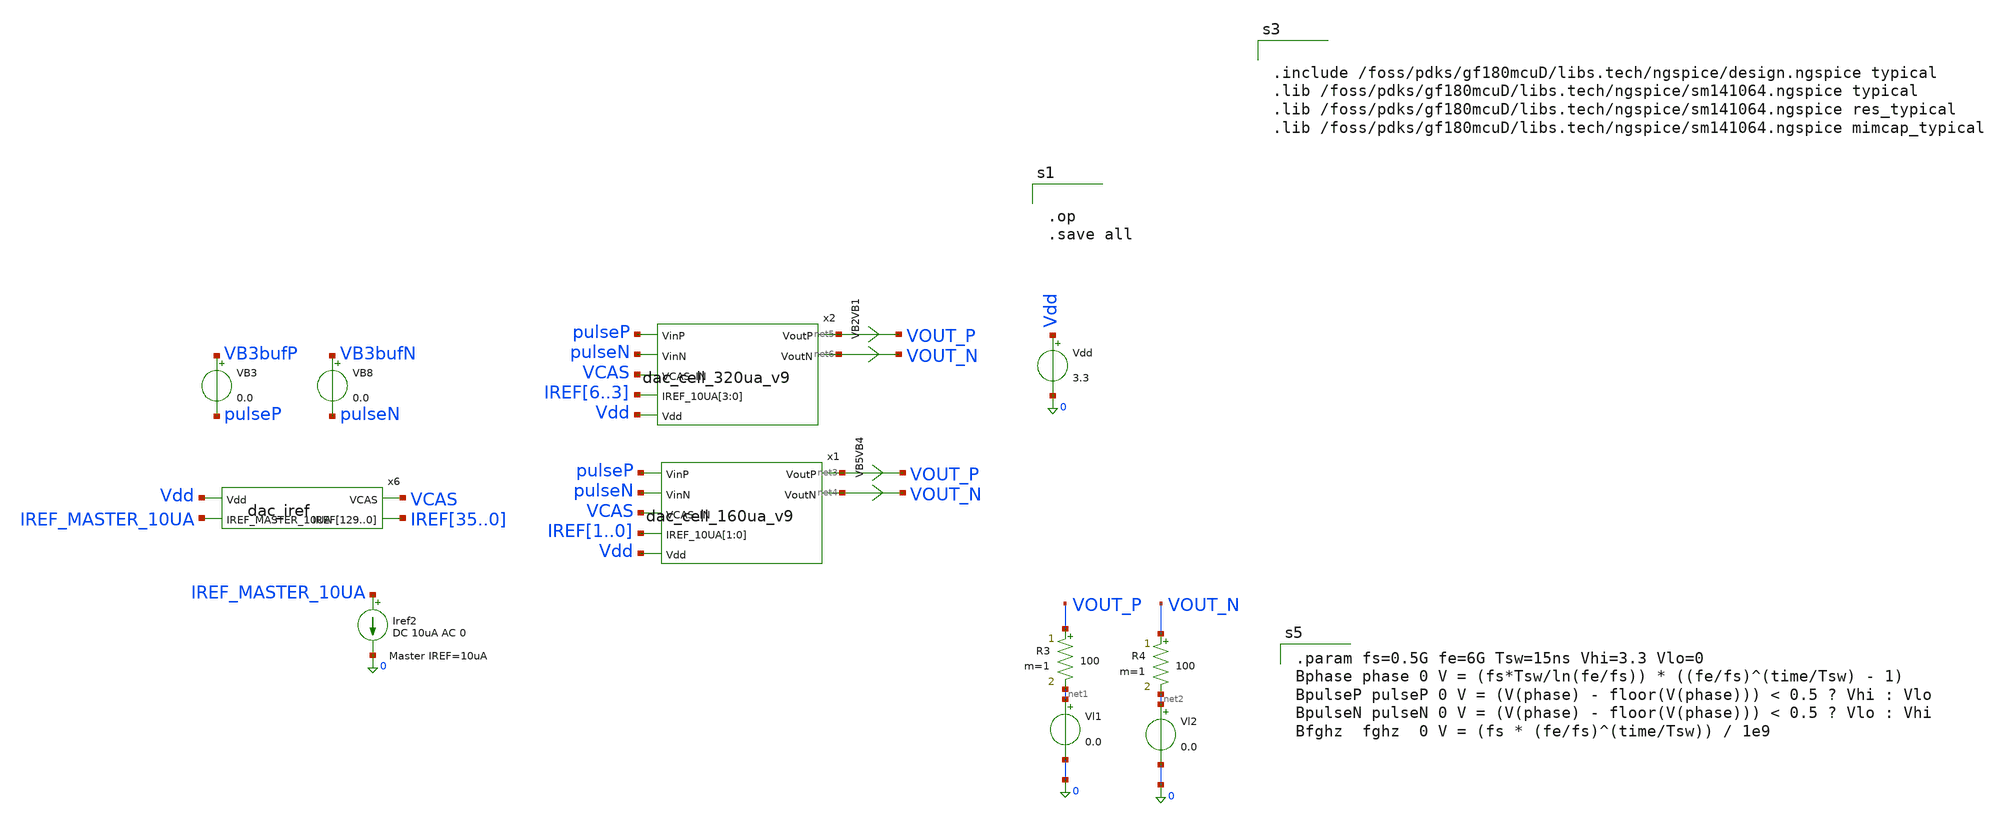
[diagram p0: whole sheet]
** sch_path: blocks/dac/test/test_dac_fsweep_160ua.sch
**.subckt test_dac_fsweep_160ua
Vdd Vdd 0 3.3
.save i(vdd)
VB3 VB3bufP pulseP 0.0
.save i(vb3)
VB8 VB3bufN pulseN 0.0
.save i(vb8)
x6 Vdd VCAS IREF35 IREF34 IREF33 IREF32 IREF31 IREF30 IREF29 IREF28 IREF27 IREF26 IREF25 IREF24
+ IREF23 IREF22 IREF21 IREF20 IREF19 IREF18 IREF17 IREF16 IREF15 IREF14 IREF13 IREF12 IREF11 IREF10 IREF9
+ IREF8 IREF7 IREF6 IREF5 IREF4 IREF3 IREF2 IREF1 IREF0 IREF35 IREF34 IREF33 IREF32 IREF31 IREF30 IREF29
+ IREF28 IREF27 IREF26 IREF25 IREF24 IREF23 IREF22 IREF21 IREF20 IREF19 IREF18 IREF17 IREF16 IREF15 IREF14
+ IREF13 IREF12 IREF11 IREF10 IREF9 IREF8 IREF7 IREF6 IREF5 IREF4 IREF3 IREF2 IREF1 IREF0 IREF35 IREF34
+ IREF33 IREF32 IREF31 IREF30 IREF29 IREF28 IREF27 IREF26 IREF25 IREF24 IREF23 IREF22 IREF21 IREF20 IREF19
+ IREF18 IREF17 IREF16 IREF15 IREF14 IREF13 IREF12 IREF11 IREF10 IREF9 IREF8 IREF7 IREF6 IREF5 IREF4 IREF3
+ IREF2 IREF1 IREF0 IREF35 IREF34 IREF33 IREF32 IREF31 IREF30 IREF29 IREF28 IREF27 IREF26 IREF25 IREF24
+ IREF23 IREF22 IREF21 IREF20 IREF19 IREF18 IREF17 IREF16 IREF15 IREF14 IREF_MASTER_10UA dac_iref
Iref2 IREF_MASTER_10UA 0 DC 10uA AC 0
R3 VOUT_P net1 100 m=1
R4 VOUT_N net2 100 m=1
Vl1 net1 0 0.0
.save i(vl1)
Vl2 net2 0 0.0
.save i(vl2)
VB4 net3 VOUT_P 0
.save i(vb4)
VB5 net4 VOUT_N 0
.save i(vb5)
x1 net3 pulseP net4 pulseN VCAS IREF1 IREF0 Vdd dac_cell_160ua_v9
VB1 net5 VOUT_P 0
.save i(vb1)
VB2 net6 VOUT_N 0
.save i(vb2)
x2 net5 pulseP net6 pulseN VCAS IREF6 IREF5 IREF4 IREF3 Vdd dac_cell_320ua_v9
**** begin user architecture code



.save all
.control

tran 1p 5ns
* plot VU1syncP+6 VU1syncN+6 VU2syncP+6 VU2syncN+6 VgN+12 VgP Dm ClkP+18 ClkN+18 i(Vl1)*5E4-6
*+ i(Vl2)*5E4-6 (i(Vl1)-i(Vl2))*5E4-12
* plot ClkP+6 ClkN+6 VU0in VB1in VU0syncP-6 VU0syncN-12 VB1syncP-6 VB1syncN-12
* plot Vout1P+15E-3 Vout1N+15E-3 Vout1P-Vout1N
* plot ClkP+5 ClkN+5 VB3syncP VB3syncN VB3bufP-5 VB3bufN-5 xb3.x1.Vg1P-10 xb3.x1.Vg1N-10
plot 3.3-xb3.x1.Vg1P 3.3-xb3.x1.Vg1N

* plot x1.x1.Vcx x1.x1.Vg1P x1.x1.Vg1N

* plot VB1syncP VB1syncN-6 VB4syncN-6 VU0bufP-12 VB1bufP-12 VB4bufP-12 VU0bufN-18 VB1bufN-18
*+ VB4bufN-18
plot i(Vl1)-i(Vl2) i(Vl1)+100E-6 i(Vl2)+100E-6

let imax = 160E-6
let imin = -160E-6
plot i(VB4)-i(VB5) imax imin
plot i(VB1)-i(VB2) i(VB4)-i(VB5) imax imin

let diff = i(Vl1)-i(Vl2)
plot pulseP diff/{imax}*5 fghz
* plot pulseP fghz



* plot i(VoutB3P)+100E-6 i(VoutB3N)+100E-6 i(VoutB3P)-i(VoutB3N) i(VoutB3N)+i(VoutB3P)
*+ i(v.x1.Vcrr1)-200E-6 i(v.x1.Vcrr2)-200E-6
* plot i(v.x1.Vcrr1) i(v.x1.Vcrr2)
* plot i(Vl1) VB1in/5E4+200E-6 VU0in/5E4+200E-6
* wrdata /foss/designs/dds/dac_isource_unary_pmos_80ua_v4_tt_500ps.csv ClkP ClkN Din VdsyncP VdsyncN
*+ i(Vl1) i(Vl2)
.endc





.op
.save all



.param fs=0.5G fe=6G Tsw=15ns Vhi=3.3 Vlo=0
Bphase phase 0 V = (fs*Tsw/ln(fe/fs)) * ((fe/fs)^(time/Tsw) - 1)
BpulseP pulseP 0 V = (V(phase) - floor(V(phase))) < 0.5 ? Vhi : Vlo
BpulseN pulseN 0 V = (V(phase) - floor(V(phase))) < 0.5 ? Vlo : Vhi
Bfghz  fghz  0 V = (fs * (fe/fs)^(time/Tsw)) / 1e9





.include /foss/pdks/gf180mcuD/libs.tech/ngspice/design.ngspice typical
.lib /foss/pdks/gf180mcuD/libs.tech/ngspice/sm141064.ngspice typical
.lib /foss/pdks/gf180mcuD/libs.tech/ngspice/sm141064.ngspice res_typical
.lib /foss/pdks/gf180mcuD/libs.tech/ngspice/sm141064.ngspice mimcap_typical


**** end user architecture code
**.ends

* expanding   symbol:  iref/dac_iref.sym # of pins=4
** sym_path: blocks/dac/iref/dac_iref.sym
** sch_path: blocks/dac/iref/dac_iref.sch
.subckt dac_iref Vdd VCAS IREF129 IREF128 IREF127 IREF126 IREF125 IREF124 IREF123 IREF122 IREF121
+ IREF120 IREF119 IREF118 IREF117 IREF116 IREF115 IREF114 IREF113 IREF112 IREF111 IREF110 IREF109 IREF108
+ IREF107 IREF106 IREF105 IREF104 IREF103 IREF102 IREF101 IREF100 IREF99 IREF98 IREF97 IREF96 IREF95 IREF94
+ IREF93 IREF92 IREF91 IREF90 IREF89 IREF88 IREF87 IREF86 IREF85 IREF84 IREF83 IREF82 IREF81 IREF80 IREF79
+ IREF78 IREF77 IREF76 IREF75 IREF74 IREF73 IREF72 IREF71 IREF70 IREF69 IREF68 IREF67 IREF66 IREF65 IREF64
+ IREF63 IREF62 IREF61 IREF60 IREF59 IREF58 IREF57 IREF56 IREF55 IREF54 IREF53 IREF52 IREF51 IREF50 IREF49
+ IREF48 IREF47 IREF46 IREF45 IREF44 IREF43 IREF42 IREF41 IREF40 IREF39 IREF38 IREF37 IREF36 IREF35 IREF34
+ IREF33 IREF32 IREF31 IREF30 IREF29 IREF28 IREF27 IREF26 IREF25 IREF24 IREF23 IREF22 IREF21 IREF20 IREF19
+ IREF18 IREF17 IREF16 IREF15 IREF14 IREF13 IREF12 IREF11 IREF10 IREF9 IREF8 IREF7 IREF6 IREF5 IREF4 IREF3
+ IREF2 IREF1 IREF0 IREF_MASTER_10UA
*.ipin Vdd
*.opin VCAS
*.opin
*+ IREF129,IREF128,IREF127,IREF126,IREF125,IREF124,IREF123,IREF122,IREF121,IREF120,IREF119,IREF118,IREF117,IREF116,IREF115,IREF114,IREF113,IREF112,IREF111,IREF110,IREF109,IREF108,IREF107,IREF106,IREF105,IREF104,IREF103,IREF102,IREF101,IREF100,IREF99,IREF98,IREF97,IREF96,IREF95,IREF94,IREF93,IREF92,IREF91,IREF90,IREF89,IREF88,IREF87,IREF86,IREF85,IREF84,IREF83,IREF82,IREF81,IREF80,IREF79,IREF78,IREF77,IREF76,IREF75,IREF74,IREF73,IREF72,IREF71,IREF70,IREF69,IREF68,IREF67,IREF66,IREF65,IREF64,IREF63,IREF62,IREF61,IREF60,IREF59,IREF58,IREF57,IREF56,IREF55,IREF54,IREF53,IREF52,IREF51,IREF50,IREF49,IREF48,IREF47,IREF46,IREF45,IREF44,IREF43,IREF42,IREF41,IREF40,IREF39,IREF38,IREF37,IREF36,IREF35,IREF34,IREF33,IREF32,IREF31,IREF30,IREF29,IREF28,IREF27,IREF26,IREF25,IREF24,IREF23,IREF22,IREF21,IREF20,IREF19,IREF18,IREF17,IREF16,IREF15,IREF14,IREF13,IREF12,IREF11,IREF10,IREF9,IREF8,IREF7,IREF6,IREF5,IREF4,IREF3,IREF2,IREF1,IREF0
*.ipin IREF_MASTER_10UA
XM69 net3 net2 0 0 nfet_03v3 L=2u W=6u nf=1 ad='int((nf+1)/2) * W/nf * 0.18u' as='int((nf+2)/2) * W/nf * 0.18u'
+ pd='2*int((nf+1)/2) * (W/nf + 0.18u)' ps='2*int((nf+2)/2) * (W/nf + 0.18u)' nrd='0.18u / W' nrs='0.18u / W'
+ sa=0 sb=0 sd=0 m=1
XM70 net2 net1 0 0 nfet_03v3 L=2u W=4u nf=1 ad='int((nf+1)/2) * W/nf * 0.18u' as='int((nf+2)/2) * W/nf * 0.18u'
+ pd='2*int((nf+1)/2) * (W/nf + 0.18u)' ps='2*int((nf+2)/2) * (W/nf + 0.18u)' nrd='0.18u / W' nrs='0.18u / W'
+ sa=0 sb=0 sd=0 m=1
XM71 net1 net4 Vdd Vdd pfet_03v3 L=2u W=6u nf=1 ad='int((nf+1)/2) * W/nf * 0.18u' as='int((nf+2)/2) * W/nf * 0.18u'
+ pd='2*int((nf+1)/2) * (W/nf + 0.18u)' ps='2*int((nf+2)/2) * (W/nf + 0.18u)' nrd='0.18u / W' nrs='0.18u / W'
+ sa=0 sb=0 sd=0 m=1
XM72 net4 net3 Vdd Vdd pfet_03v3 L=2u W=5u nf=1 ad='int((nf+1)/2) * W/nf * 0.18u' as='int((nf+2)/2) * W/nf * 0.18u'
+ pd='2*int((nf+1)/2) * (W/nf + 0.18u)' ps='2*int((nf+2)/2) * (W/nf + 0.18u)' nrd='0.18u / W' nrs='0.18u / W'
+ sa=0 sb=0 sd=0 m=1
x1 Vdd VCAS net4 VCAS IB_10UA ota5t
XC7 net4 0 cap_mim_2f0_m3m4_noshield c_width=5e-6 c_length=5e-6 m=1
XM7 VPg1 VPg1 Vdd Vdd pfet_03v3 L=1u W=6u nf=1 ad='int((nf+1)/2) * W/nf * 0.18u' as='int((nf+2)/2) * W/nf * 0.18u'
+ pd='2*int((nf+1)/2) * (W/nf + 0.18u)' ps='2*int((nf+2)/2) * (W/nf + 0.18u)' nrd='0.18u / W' nrs='0.18u / W'
+ sa=0 sb=0 sd=0 m=1
XM8 IREF_MASTER_10UA IREF_MASTER_10UA VPg1 Vdd pfet_03v3 L=1u W=6u nf=1 ad='int((nf+1)/2) * W/nf * 0.18u'
+ as='int((nf+2)/2) * W/nf * 0.18u' pd='2*int((nf+1)/2) * (W/nf + 0.18u)' ps='2*int((nf+2)/2) * (W/nf + 0.18u)'
+ nrd='0.18u / W' nrs='0.18u / W' sa=0 sb=0 sd=0 m=1
XM9 net5 VPg1 Vdd Vdd pfet_03v3 L=1u W=6u nf=1 ad='int((nf+1)/2) * W/nf * 0.18u' as='int((nf+2)/2) * W/nf * 0.18u'
+ pd='2*int((nf+1)/2) * (W/nf + 0.18u)' ps='2*int((nf+2)/2) * (W/nf + 0.18u)' nrd='0.18u / W' nrs='0.18u / W'
+ sa=0 sb=0 sd=0 m=1
XM10 VNMir IREF_MASTER_10UA net5 Vdd pfet_03v3 L=1u W=6u nf=1 ad='int((nf+1)/2) * W/nf * 0.18u' as='int((nf+2)/2) * W/nf * 0.18u'
+ pd='2*int((nf+1)/2) * (W/nf + 0.18u)' ps='2*int((nf+2)/2) * (W/nf + 0.18u)' nrd='0.18u / W' nrs='0.18u / W'
+ sa=0 sb=0 sd=0 m=1
XM11 VNMir VNMir 0 0 nfet_03v3 L=4u W=4u nf=1 ad='int((nf+1)/2) * W/nf * 0.18u' as='int((nf+2)/2) * W/nf * 0.18u'
+ pd='2*int((nf+1)/2) * (W/nf + 0.18u)' ps='2*int((nf+2)/2) * (W/nf + 0.18u)' nrd='0.18u / W' nrs='0.18u / W'
+ sa=0 sb=0 sd=0 m=1
XM12 net6 VPg1 Vdd Vdd pfet_03v3 L=1u W=6u nf=1 ad='int((nf+1)/2) * W/nf * 0.18u' as='int((nf+2)/2) * W/nf * 0.18u'
+ pd='2*int((nf+1)/2) * (W/nf + 0.18u)' ps='2*int((nf+2)/2) * (W/nf + 0.18u)' nrd='0.18u / W' nrs='0.18u / W'
+ sa=0 sb=0 sd=0 m=1
XM14 VNCas IREF_MASTER_10UA net6 Vdd pfet_03v3 L=1u W=6u nf=1 ad='int((nf+1)/2) * W/nf * 0.18u' as='int((nf+2)/2) * W/nf * 0.18u'
+ pd='2*int((nf+1)/2) * (W/nf + 0.18u)' ps='2*int((nf+2)/2) * (W/nf + 0.18u)' nrd='0.18u / W' nrs='0.18u / W'
+ sa=0 sb=0 sd=0 m=1
XM16 net7 VNCas 0 0 nfet_03v3 L={repL} W={repW} nf=1 ad='int((nf+1)/2) * W/nf * 0.18u' as='int((nf+2)/2) * W/nf * 0.18u'
+ pd='2*int((nf+1)/2) * (W/nf + 0.18u)' ps='2*int((nf+2)/2) * (W/nf + 0.18u)' nrd='0.18u / W' nrs='0.18u / W'
+ sa=0 sb=0 sd=0 m=1
XM17 VNCas VNMir net7 0 nfet_03v3 L={repL} W={repW} nf=1 ad='int((nf+1)/2) * W/nf * 0.18u' as='int((nf+2)/2) * W/nf * 0.18u'
+ pd='2*int((nf+1)/2) * (W/nf + 0.18u)' ps='2*int((nf+2)/2) * (W/nf + 0.18u)' nrd='0.18u / W' nrs='0.18u / W'
+ sa=0 sb=0 sd=0 m=1
XM4 net9 VNMir net8 0 nfet_03v3 L={repL} W={repW} nf=1 ad='int((nf+1)/2) * W/nf * 0.18u' as='int((nf+2)/2) * W/nf * 0.18u'
+ pd='2*int((nf+1)/2) * (W/nf + 0.18u)' ps='2*int((nf+2)/2) * (W/nf + 0.18u)' nrd='0.18u / W' nrs='0.18u / W'
+ sa=0 sb=0 sd=0 m=1
XM5 net9 net9 Vdd Vdd pfet_03v3 L=1u W=8u nf=1 ad='int((nf+1)/2) * W/nf * 0.18u' as='int((nf+2)/2) * W/nf * 0.18u'
+ pd='2*int((nf+1)/2) * (W/nf + 0.18u)' ps='2*int((nf+2)/2) * (W/nf + 0.18u)' nrd='0.18u / W' nrs='0.18u / W'
+ sa=0 sb=0 sd=0 m=1
XM13 net8 VNCas 0 0 nfet_03v3 L={repL} W={repW} nf=1 ad='int((nf+1)/2) * W/nf * 0.18u' as='int((nf+2)/2) * W/nf * 0.18u'
+ pd='2*int((nf+1)/2) * (W/nf + 0.18u)' ps='2*int((nf+2)/2) * (W/nf + 0.18u)' nrd='0.18u / W' nrs='0.18u / W'
+ sa=0 sb=0 sd=0 m=1
XR3 net4 net3 Vdd ppolyf_u_1k r_width=1e-6 r_length=4e-6 m=1
XR2 net1 net2 Vdd ppolyf_u_1k r_width=1e-6 r_length=8e-6 m=1
.param repW=4u
.param repL=1u
XM15 IB_10UA net9 Vdd Vdd pfet_03v3 L=1u W=8u nf=1 ad='int((nf+1)/2) * W/nf * 0.18u' as='int((nf+2)/2) * W/nf * 0.18u'
+ pd='2*int((nf+1)/2) * (W/nf + 0.18u)' ps='2*int((nf+2)/2) * (W/nf + 0.18u)' nrd='0.18u / W' nrs='0.18u / W'
+ sa=0 sb=0 sd=0 m=2
x2[129] VNMir IREF129 VNCas dac_mirror
x2[128] VNMir IREF128 VNCas dac_mirror
x2[127] VNMir IREF127 VNCas dac_mirror
x2[126] VNMir IREF126 VNCas dac_mirror
x2[125] VNMir IREF125 VNCas dac_mirror
x2[124] VNMir IREF124 VNCas dac_mirror
x2[123] VNMir IREF123 VNCas dac_mirror
x2[122] VNMir IREF122 VNCas dac_mirror
x2[121] VNMir IREF121 VNCas dac_mirror
x2[120] VNMir IREF120 VNCas dac_mirror
x2[119] VNMir IREF119 VNCas dac_mirror
x2[118] VNMir IREF118 VNCas dac_mirror
x2[117] VNMir IREF117 VNCas dac_mirror
x2[116] VNMir IREF116 VNCas dac_mirror
x2[115] VNMir IREF115 VNCas dac_mirror
x2[114] VNMir IREF114 VNCas dac_mirror
x2[113] VNMir IREF113 VNCas dac_mirror
x2[112] VNMir IREF112 VNCas dac_mirror
x2[111] VNMir IREF111 VNCas dac_mirror
x2[110] VNMir IREF110 VNCas dac_mirror
x2[109] VNMir IREF109 VNCas dac_mirror
x2[108] VNMir IREF108 VNCas dac_mirror
x2[107] VNMir IREF107 VNCas dac_mirror
x2[106] VNMir IREF106 VNCas dac_mirror
x2[105] VNMir IREF105 VNCas dac_mirror
x2[104] VNMir IREF104 VNCas dac_mirror
x2[103] VNMir IREF103 VNCas dac_mirror
x2[102] VNMir IREF102 VNCas dac_mirror
x2[101] VNMir IREF101 VNCas dac_mirror
x2[100] VNMir IREF100 VNCas dac_mirror
x2[99] VNMir IREF99 VNCas dac_mirror
x2[98] VNMir IREF98 VNCas dac_mirror
x2[97] VNMir IREF97 VNCas dac_mirror
x2[96] VNMir IREF96 VNCas dac_mirror
x2[95] VNMir IREF95 VNCas dac_mirror
x2[94] VNMir IREF94 VNCas dac_mirror
x2[93] VNMir IREF93 VNCas dac_mirror
x2[92] VNMir IREF92 VNCas dac_mirror
x2[91] VNMir IREF91 VNCas dac_mirror
x2[90] VNMir IREF90 VNCas dac_mirror
x2[89] VNMir IREF89 VNCas dac_mirror
x2[88] VNMir IREF88 VNCas dac_mirror
x2[87] VNMir IREF87 VNCas dac_mirror
x2[86] VNMir IREF86 VNCas dac_mirror
x2[85] VNMir IREF85 VNCas dac_mirror
x2[84] VNMir IREF84 VNCas dac_mirror
x2[83] VNMir IREF83 VNCas dac_mirror
x2[82] VNMir IREF82 VNCas dac_mirror
x2[81] VNMir IREF81 VNCas dac_mirror
x2[80] VNMir IREF80 VNCas dac_mirror
x2[79] VNMir IREF79 VNCas dac_mirror
x2[78] VNMir IREF78 VNCas dac_mirror
x2[77] VNMir IREF77 VNCas dac_mirror
x2[76] VNMir IREF76 VNCas dac_mirror
x2[75] VNMir IREF75 VNCas dac_mirror
x2[74] VNMir IREF74 VNCas dac_mirror
x2[73] VNMir IREF73 VNCas dac_mirror
x2[72] VNMir IREF72 VNCas dac_mirror
x2[71] VNMir IREF71 VNCas dac_mirror
x2[70] VNMir IREF70 VNCas dac_mirror
x2[69] VNMir IREF69 VNCas dac_mirror
x2[68] VNMir IREF68 VNCas dac_mirror
x2[67] VNMir IREF67 VNCas dac_mirror
x2[66] VNMir IREF66 VNCas dac_mirror
x2[65] VNMir IREF65 VNCas dac_mirror
x2[64] VNMir IREF64 VNCas dac_mirror
x2[63] VNMir IREF63 VNCas dac_mirror
x2[62] VNMir IREF62 VNCas dac_mirror
x2[61] VNMir IREF61 VNCas dac_mirror
x2[60] VNMir IREF60 VNCas dac_mirror
x2[59] VNMir IREF59 VNCas dac_mirror
x2[58] VNMir IREF58 VNCas dac_mirror
x2[57] VNMir IREF57 VNCas dac_mirror
x2[56] VNMir IREF56 VNCas dac_mirror
x2[55] VNMir IREF55 VNCas dac_mirror
x2[54] VNMir IREF54 VNCas dac_mirror
x2[53] VNMir IREF53 VNCas dac_mirror
x2[52] VNMir IREF52 VNCas dac_mirror
x2[51] VNMir IREF51 VNCas dac_mirror
x2[50] VNMir IREF50 VNCas dac_mirror
x2[49] VNMir IREF49 VNCas dac_mirror
x2[48] VNMir IREF48 VNCas dac_mirror
x2[47] VNMir IREF47 VNCas dac_mirror
x2[46] VNMir IREF46 VNCas dac_mirror
x2[45] VNMir IREF45 VNCas dac_mirror
x2[44] VNMir IREF44 VNCas dac_mirror
x2[43] VNMir IREF43 VNCas dac_mirror
x2[42] VNMir IREF42 VNCas dac_mirror
x2[41] VNMir IREF41 VNCas dac_mirror
x2[40] VNMir IREF40 VNCas dac_mirror
x2[39] VNMir IREF39 VNCas dac_mirror
x2[38] VNMir IREF38 VNCas dac_mirror
x2[37] VNMir IREF37 VNCas dac_mirror
x2[36] VNMir IREF36 VNCas dac_mirror
x2[35] VNMir IREF35 VNCas dac_mirror
x2[34] VNMir IREF34 VNCas dac_mirror
x2[33] VNMir IREF33 VNCas dac_mirror
x2[32] VNMir IREF32 VNCas dac_mirror
x2[31] VNMir IREF31 VNCas dac_mirror
x2[30] VNMir IREF30 VNCas dac_mirror
x2[29] VNMir IREF29 VNCas dac_mirror
x2[28] VNMir IREF28 VNCas dac_mirror
x2[27] VNMir IREF27 VNCas dac_mirror
x2[26] VNMir IREF26 VNCas dac_mirror
x2[25] VNMir IREF25 VNCas dac_mirror
x2[24] VNMir IREF24 VNCas dac_mirror
x2[23] VNMir IREF23 VNCas dac_mirror
x2[22] VNMir IREF22 VNCas dac_mirror
x2[21] VNMir IREF21 VNCas dac_mirror
x2[20] VNMir IREF20 VNCas dac_mirror
x2[19] VNMir IREF19 VNCas dac_mirror
x2[18] VNMir IREF18 VNCas dac_mirror
x2[17] VNMir IREF17 VNCas dac_mirror
x2[16] VNMir IREF16 VNCas dac_mirror
x2[15] VNMir IREF15 VNCas dac_mirror
x2[14] VNMir IREF14 VNCas dac_mirror
x2[13] VNMir IREF13 VNCas dac_mirror
x2[12] VNMir IREF12 VNCas dac_mirror
x2[11] VNMir IREF11 VNCas dac_mirror
x2[10] VNMir IREF10 VNCas dac_mirror
x2[9] VNMir IREF9 VNCas dac_mirror
x2[8] VNMir IREF8 VNCas dac_mirror
x2[7] VNMir IREF7 VNCas dac_mirror
x2[6] VNMir IREF6 VNCas dac_mirror
x2[5] VNMir IREF5 VNCas dac_mirror
x2[4] VNMir IREF4 VNCas dac_mirror
x2[3] VNMir IREF3 VNCas dac_mirror
x2[2] VNMir IREF2 VNCas dac_mirror
x2[1] VNMir IREF1 VNCas dac_mirror
x2[0] VNMir IREF0 VNCas dac_mirror
.ends


* expanding   symbol:  cellv9/dac_cell_160ua_v9.sym # of pins=7
** sym_path: blocks/dac/cellv9/dac_cell_160ua_v9.sym
** sch_path: blocks/dac/cellv9/dac_cell_160ua_v9.sch
.subckt dac_cell_160ua_v9 VoutP VinP VoutN VinN VCAS_IN IREF_10UA[1] IREF_10UA[0] Vdd
*.opin VoutP
*.opin VoutN
*.ipin VinP
*.ipin VinN
*.ipin Vdd
*.ipin VCAS_IN
*.ipin IREF_10UA[1],IREF_10UA[0]
x1[1] net1[1] net2[1] net3[1] net4[1] net5[1] net6[1] net7[1] net8[1] dac_cell_80ua_v9
x1[0] net1[0] net2[0] net3[0] net4[0] net5[0] net6[0] net7[0] net8[0] dac_cell_80ua_v9
.ends


* expanding   symbol:  cellv9/dac_cell_320ua_v9.sym # of pins=7
** sym_path: blocks/dac/cellv9/dac_cell_320ua_v9.sym
** sch_path: blocks/dac/cellv9/dac_cell_320ua_v9.sch
.subckt dac_cell_320ua_v9 VoutP VinP VoutN VinN VCAS_IN IREF_10UA[3] IREF_10UA[2] IREF_10UA[1]
+ IREF_10UA[0] Vdd
*.opin VoutP
*.opin VoutN
*.ipin VinP
*.ipin VinN
*.ipin Vdd
*.ipin VCAS_IN
*.ipin IREF_10UA[3],IREF_10UA[2],IREF_10UA[1],IREF_10UA[0]
x1[3] net1[3] net2[3] net3[3] net4[3] net5[3] net6[3] net7[3] net8[3] dac_cell_80ua_v9
x1[2] net1[2] net2[2] net3[2] net4[2] net5[2] net6[2] net7[2] net8[2] dac_cell_80ua_v9
x1[1] net1[1] net2[1] net3[1] net4[1] net5[1] net6[1] net7[1] net8[1] dac_cell_80ua_v9
x1[0] net1[0] net2[0] net3[0] net4[0] net5[0] net6[0] net7[0] net8[0] dac_cell_80ua_v9
.ends


* expanding   symbol:  common/ota5t.sym # of pins=5
** sym_path: blocks/dac/common/ota5t.sym
** sch_path: blocks/dac/common/ota5t.sch
.subckt ota5t Vdd VIN_N VIN_P VOUT IB_10UA
*.ipin VIN_P
*.ipin VIN_N
*.opin VOUT
*.ipin Vdd
*.ipin IB_10UA
XM16 VOUT net1 0 0 nfet_03v3 L=1u W=2u nf=1 ad='int((nf+1)/2) * W/nf * 0.18u' as='int((nf+2)/2) * W/nf * 0.18u'
+ pd='2*int((nf+1)/2) * (W/nf + 0.18u)' ps='2*int((nf+2)/2) * (W/nf + 0.18u)' nrd='0.18u / W' nrs='0.18u / W'
+ sa=0 sb=0 sd=0 m=1
XM1 VOUT VIN_N IB_10UA Vdd pfet_03v3 L=1u W=4u nf=1 ad='int((nf+1)/2) * W/nf * 0.18u' as='int((nf+2)/2) * W/nf * 0.18u'
+ pd='2*int((nf+1)/2) * (W/nf + 0.18u)' ps='2*int((nf+2)/2) * (W/nf + 0.18u)' nrd='0.18u / W' nrs='0.18u / W'
+ sa=0 sb=0 sd=0 m=1
XM19 net1 VIN_P IB_10UA Vdd pfet_03v3 L=1u W=4u nf=1 ad='int((nf+1)/2) * W/nf * 0.18u' as='int((nf+2)/2) * W/nf * 0.18u'
+ pd='2*int((nf+1)/2) * (W/nf + 0.18u)' ps='2*int((nf+2)/2) * (W/nf + 0.18u)' nrd='0.18u / W' nrs='0.18u / W'
+ sa=0 sb=0 sd=0 m=1
XM22 net1 net1 0 0 nfet_03v3 L=1u W=2u nf=1 ad='int((nf+1)/2) * W/nf * 0.18u' as='int((nf+2)/2) * W/nf * 0.18u'
+ pd='2*int((nf+1)/2) * (W/nf + 0.18u)' ps='2*int((nf+2)/2) * (W/nf + 0.18u)' nrd='0.18u / W' nrs='0.18u / W'
+ sa=0 sb=0 sd=0 m=1
.ends


* expanding   symbol:  iref/dac_mirror.sym # of pins=3
** sym_path: blocks/dac/iref/dac_mirror.sym
** sch_path: blocks/dac/iref/dac_mirror.sch
.subckt dac_mirror VN_MIR IREF VN_CAS
*.ipin VN_MIR
*.opin IREF
*.ipin VN_CAS
XM1 IREF VN_MIR net1 0 nfet_03v3 L={repL} W={repW} nf=1 ad='int((nf+1)/2) * W/nf * 0.18u' as='int((nf+2)/2) * W/nf * 0.18u'
+ pd='2*int((nf+1)/2) * (W/nf + 0.18u)' ps='2*int((nf+2)/2) * (W/nf + 0.18u)' nrd='0.18u / W' nrs='0.18u / W'
+ sa=0 sb=0 sd=0 m=1
XM2 net1 VN_CAS 0 0 nfet_03v3 L={repL} W={repW} nf=1 ad='int((nf+1)/2) * W/nf * 0.18u' as='int((nf+2)/2) * W/nf * 0.18u'
+ pd='2*int((nf+1)/2) * (W/nf + 0.18u)' ps='2*int((nf+2)/2) * (W/nf + 0.18u)' nrd='0.18u / W' nrs='0.18u / W'
+ sa=0 sb=0 sd=0 m=1
.ends


* expanding   symbol:  cellv9/dac_cell_80ua_v9.sym # of pins=8
** sym_path: blocks/dac/cellv9/dac_cell_80ua_v9.sym
** sch_path: blocks/dac/cellv9/dac_cell_80ua_v9.sch
.subckt dac_cell_80ua_v9 VoutP VinP VoutN VinN VPCas VNCas VNMir Vdd
*.opin VoutP
*.opin VoutN
*.ipin VinP
*.ipin VinN
*.ipin Vdd
*.ipin VPCas
*.ipin VNCas
*.ipin VNMir
.param cmLw=0.4u
.param cmHw=0.7u
.param cmLfbw=1.0u
.param cmHfbw=0.22u
XM20 VxP Vg1P Vcx Vdd pfet_03v3 L=0.28u W={cswW} nf=1 ad='int((nf+1)/2) * W/nf * 0.18u' as='int((nf+2)/2) * W/nf * 0.18u'
+ pd='2*int((nf+1)/2) * (W/nf + 0.18u)' ps='2*int((nf+2)/2) * (W/nf + 0.18u)' nrd='0.18u / W' nrs='0.18u / W'
+ sa=0 sb=0 sd=0 m=1
XM21 VxN Vg1N Vcx Vdd pfet_03v3 L=0.28u W={cswW} nf=1 ad='int((nf+1)/2) * W/nf * 0.18u' as='int((nf+2)/2) * W/nf * 0.18u'
+ pd='2*int((nf+1)/2) * (W/nf + 0.18u)' ps='2*int((nf+2)/2) * (W/nf + 0.18u)' nrd='0.18u / W' nrs='0.18u / W'
+ sa=0 sb=0 sd=0 m=1
XM22 VoutP VcbP VxP Vdd pfet_03v3 L=0.28u W={cbufW} nf=1 ad='int((nf+1)/2) * W/nf * 0.18u' as='int((nf+2)/2) * W/nf * 0.18u'
+ pd='2*int((nf+1)/2) * (W/nf + 0.18u)' ps='2*int((nf+2)/2) * (W/nf + 0.18u)' nrd='0.18u / W' nrs='0.18u / W'
+ sa=0 sb=0 sd=0 m=1
XM23 VoutN VcbN VxN Vdd pfet_03v3 L=0.28u W={cbufW} nf=1 ad='int((nf+1)/2) * W/nf * 0.18u' as='int((nf+2)/2) * W/nf * 0.18u'
+ pd='2*int((nf+1)/2) * (W/nf + 0.18u)' ps='2*int((nf+2)/2) * (W/nf + 0.18u)' nrd='0.18u / W' nrs='0.18u / W'
+ sa=0 sb=0 sd=0 m=1
XM24 net1 Vg1N Vdd Vdd pfet_03v3 L=0.28u W={invPw} nf=1 ad='int((nf+1)/2) * W/nf * 0.18u' as='int((nf+2)/2) * W/nf * 0.18u'
+ pd='2*int((nf+1)/2) * (W/nf + 0.18u)' ps='2*int((nf+2)/2) * (W/nf + 0.18u)' nrd='0.18u / W' nrs='0.18u / W'
+ sa=0 sb=0 sd=0 m=1
XM34 net1 Vg1N 0 0 nfet_03v3 L=0.28u W=0.22u nf=1 ad='int((nf+1)/2) * W/nf * 0.18u' as='int((nf+2)/2) * W/nf * 0.18u'
+ pd='2*int((nf+1)/2) * (W/nf + 0.18u)' ps='2*int((nf+2)/2) * (W/nf + 0.18u)' nrd='0.18u / W' nrs='0.18u / W'
+ sa=0 sb=0 sd=0 m=1
XM35 VoutN net1 VoutN Vdd pfet_03v3 L=0.28u W={dummyW} nf=1 ad='int((nf+1)/2) * W/nf * 0.18u' as='int((nf+2)/2) * W/nf * 0.18u'
+ pd='2*int((nf+1)/2) * (W/nf + 0.18u)' ps='2*int((nf+2)/2) * (W/nf + 0.18u)' nrd='0.18u / W' nrs='0.18u / W'
+ sa=0 sb=0 sd=0 m=1
XM36 net2 Vg1P Vdd Vdd pfet_03v3 L=0.28u W={invPw} nf=1 ad='int((nf+1)/2) * W/nf * 0.18u' as='int((nf+2)/2) * W/nf * 0.18u'
+ pd='2*int((nf+1)/2) * (W/nf + 0.18u)' ps='2*int((nf+2)/2) * (W/nf + 0.18u)' nrd='0.18u / W' nrs='0.18u / W'
+ sa=0 sb=0 sd=0 m=1
XM37 net2 Vg1P 0 0 nfet_03v3 L=0.28u W=0.22u nf=1 ad='int((nf+1)/2) * W/nf * 0.18u' as='int((nf+2)/2) * W/nf * 0.18u'
+ pd='2*int((nf+1)/2) * (W/nf + 0.18u)' ps='2*int((nf+2)/2) * (W/nf + 0.18u)' nrd='0.18u / W' nrs='0.18u / W'
+ sa=0 sb=0 sd=0 m=1
XM38 VoutP net2 VoutP Vdd pfet_03v3 L=0.28u W={dummyW} nf=1 ad='int((nf+1)/2) * W/nf * 0.18u' as='int((nf+2)/2) * W/nf * 0.18u'
+ pd='2*int((nf+1)/2) * (W/nf + 0.18u)' ps='2*int((nf+2)/2) * (W/nf + 0.18u)' nrd='0.18u / W' nrs='0.18u / W'
+ sa=0 sb=0 sd=0 m=1
VcbRef3 VcbRef 0 {Vcbias}
.save i(vcbref3)
.param VcBias=0.84
.param casW=4u
XM39 net3 VinPDr VH Vdd pfet_03v3 L=0.28u W={cmHw} nf=1 ad='int((nf+1)/2) * W/nf * 0.18u' as='int((nf+2)/2) * W/nf * 0.18u'
+ pd='2*int((nf+1)/2) * (W/nf + 0.18u)' ps='2*int((nf+2)/2) * (W/nf + 0.18u)' nrd='0.18u / W' nrs='0.18u / W'
+ sa=0 sb=0 sd=0 m=1
XM40 Vg1P VinPDr net3 Vdd pfet_03v3 L=0.28u W={cmHw} nf=1 ad='int((nf+1)/2) * W/nf * 0.18u' as='int((nf+2)/2) * W/nf * 0.18u'
+ pd='2*int((nf+1)/2) * (W/nf + 0.18u)' ps='2*int((nf+2)/2) * (W/nf + 0.18u)' nrd='0.18u / W' nrs='0.18u / W'
+ sa=0 sb=0 sd=0 m=1
XM41 Vg1P VinPDr VL 0 nfet_03v3 L=0.28u W={cmLw} nf=1 ad='int((nf+1)/2) * W/nf * 0.18u' as='int((nf+2)/2) * W/nf * 0.18u'
+ pd='2*int((nf+1)/2) * (W/nf + 0.18u)' ps='2*int((nf+2)/2) * (W/nf + 0.18u)' nrd='0.18u / W' nrs='0.18u / W'
+ sa=0 sb=0 sd=0 m=1
XM42 net3 VinNDr VH Vdd pfet_03v3 L=0.28u W={cmHfbW} nf=1 ad='int((nf+1)/2) * W/nf * 0.18u' as='int((nf+2)/2) * W/nf * 0.18u'
+ pd='2*int((nf+1)/2) * (W/nf + 0.18u)' ps='2*int((nf+2)/2) * (W/nf + 0.18u)' nrd='0.18u / W' nrs='0.18u / W'
+ sa=0 sb=0 sd=0 m=1
XM43 net4 VinNDr VH Vdd pfet_03v3 L=0.28u W={cmHw} nf=1 ad='int((nf+1)/2) * W/nf * 0.18u' as='int((nf+2)/2) * W/nf * 0.18u'
+ pd='2*int((nf+1)/2) * (W/nf + 0.18u)' ps='2*int((nf+2)/2) * (W/nf + 0.18u)' nrd='0.18u / W' nrs='0.18u / W'
+ sa=0 sb=0 sd=0 m=1
XM44 Vg1N VinNDr net4 Vdd pfet_03v3 L=0.28u W={cmHw} nf=1 ad='int((nf+1)/2) * W/nf * 0.18u' as='int((nf+2)/2) * W/nf * 0.18u'
+ pd='2*int((nf+1)/2) * (W/nf + 0.18u)' ps='2*int((nf+2)/2) * (W/nf + 0.18u)' nrd='0.18u / W' nrs='0.18u / W'
+ sa=0 sb=0 sd=0 m=1
XM45 Vg1N VinNDr VL 0 nfet_03v3 L=0.28u W={cmLw} nf=1 ad='int((nf+1)/2) * W/nf * 0.18u' as='int((nf+2)/2) * W/nf * 0.18u'
+ pd='2*int((nf+1)/2) * (W/nf + 0.18u)' ps='2*int((nf+2)/2) * (W/nf + 0.18u)' nrd='0.18u / W' nrs='0.18u / W'
+ sa=0 sb=0 sd=0 m=1
XM46 net4 VinPDr VH Vdd pfet_03v3 L=0.28u W={cmHfbW} nf=1 ad='int((nf+1)/2) * W/nf * 0.18u' as='int((nf+2)/2) * W/nf * 0.18u'
+ pd='2*int((nf+1)/2) * (W/nf + 0.18u)' ps='2*int((nf+2)/2) * (W/nf + 0.18u)' nrd='0.18u / W' nrs='0.18u / W'
+ sa=0 sb=0 sd=0 m=1
XM47 VL VinPDr Vg1N Vdd pfet_03v3 L=0.28u W={cmLfbw} nf=1 ad='int((nf+1)/2) * W/nf * 0.18u' as='int((nf+2)/2) * W/nf * 0.18u'
+ pd='2*int((nf+1)/2) * (W/nf + 0.18u)' ps='2*int((nf+2)/2) * (W/nf + 0.18u)' nrd='0.18u / W' nrs='0.18u / W'
+ sa=0 sb=0 sd=0 m=1
XM48 VL VinNDr Vg1P Vdd pfet_03v3 L=0.28u W={cmLfbw} nf=1 ad='int((nf+1)/2) * W/nf * 0.18u' as='int((nf+2)/2) * W/nf * 0.18u'
+ pd='2*int((nf+1)/2) * (W/nf + 0.18u)' ps='2*int((nf+2)/2) * (W/nf + 0.18u)' nrd='0.18u / W' nrs='0.18u / W'
+ sa=0 sb=0 sd=0 m=1
.param dummyW=1.0u
.param invPW=0.5u
.param cswW=3.0u
.param cbufW=3.2u
x1 VH Vdd VL clamp
.param mirW=4u
.param mirL=1u
.param casL=1u
XM4 net5 VPCas Vdd Vdd pfet_03v3 L={casL} W={casW} nf=1 ad='int((nf+1)/2) * W/nf * 0.18u' as='int((nf+2)/2) * W/nf * 0.18u'
+ pd='2*int((nf+1)/2) * (W/nf + 0.18u)' ps='2*int((nf+2)/2) * (W/nf + 0.18u)' nrd='0.18u / W' nrs='0.18u / W'
+ sa=0 sb=0 sd=0 m=1
XM7 Vcx VPMir net5 Vdd pfet_03v3 L={mirL} W={mirW} nf=1 ad='int((nf+1)/2) * W/nf * 0.18u' as='int((nf+2)/2) * W/nf * 0.18u'
+ pd='2*int((nf+1)/2) * (W/nf + 0.18u)' ps='2*int((nf+2)/2) * (W/nf + 0.18u)' nrd='0.18u / W' nrs='0.18u / W'
+ sa=0 sb=0 sd=0 m=1
XM9 net6 VPCas Vdd Vdd pfet_03v3 L={casL} W={casW} nf=1 ad='int((nf+1)/2) * W/nf * 0.18u' as='int((nf+2)/2) * W/nf * 0.18u'
+ pd='2*int((nf+1)/2) * (W/nf + 0.18u)' ps='2*int((nf+2)/2) * (W/nf + 0.18u)' nrd='0.18u / W' nrs='0.18u / W'
+ sa=0 sb=0 sd=0 m=1
XM10 Vcx VPMir net6 Vdd pfet_03v3 L={mirL} W={mirW} nf=1 ad='int((nf+1)/2) * W/nf * 0.18u' as='int((nf+2)/2) * W/nf * 0.18u'
+ pd='2*int((nf+1)/2) * (W/nf + 0.18u)' ps='2*int((nf+2)/2) * (W/nf + 0.18u)' nrd='0.18u / W' nrs='0.18u / W'
+ sa=0 sb=0 sd=0 m=1
XM11 net7 VPCas Vdd Vdd pfet_03v3 L={casL} W={casW} nf=1 ad='int((nf+1)/2) * W/nf * 0.18u' as='int((nf+2)/2) * W/nf * 0.18u'
+ pd='2*int((nf+1)/2) * (W/nf + 0.18u)' ps='2*int((nf+2)/2) * (W/nf + 0.18u)' nrd='0.18u / W' nrs='0.18u / W'
+ sa=0 sb=0 sd=0 m=1
XM12 Vcx VPMir net7 Vdd pfet_03v3 L={mirL} W={mirW} nf=1 ad='int((nf+1)/2) * W/nf * 0.18u' as='int((nf+2)/2) * W/nf * 0.18u'
+ pd='2*int((nf+1)/2) * (W/nf + 0.18u)' ps='2*int((nf+2)/2) * (W/nf + 0.18u)' nrd='0.18u / W' nrs='0.18u / W'
+ sa=0 sb=0 sd=0 m=1
XM13 net8 VPCas Vdd Vdd pfet_03v3 L={casL} W={casW} nf=1 ad='int((nf+1)/2) * W/nf * 0.18u' as='int((nf+2)/2) * W/nf * 0.18u'
+ pd='2*int((nf+1)/2) * (W/nf + 0.18u)' ps='2*int((nf+2)/2) * (W/nf + 0.18u)' nrd='0.18u / W' nrs='0.18u / W'
+ sa=0 sb=0 sd=0 m=1
XM14 Vcx VPMir net8 Vdd pfet_03v3 L={mirL} W={mirW} nf=1 ad='int((nf+1)/2) * W/nf * 0.18u' as='int((nf+2)/2) * W/nf * 0.18u'
+ pd='2*int((nf+1)/2) * (W/nf + 0.18u)' ps='2*int((nf+2)/2) * (W/nf + 0.18u)' nrd='0.18u / W' nrs='0.18u / W'
+ sa=0 sb=0 sd=0 m=1
XM1 net9 VPCas Vdd Vdd pfet_03v3 L={casL} W={casW} nf=1 ad='int((nf+1)/2) * W/nf * 0.18u' as='int((nf+2)/2) * W/nf * 0.18u'
+ pd='2*int((nf+1)/2) * (W/nf + 0.18u)' ps='2*int((nf+2)/2) * (W/nf + 0.18u)' nrd='0.18u / W' nrs='0.18u / W'
+ sa=0 sb=0 sd=0 m=1
XM5 Vcx VPMir net9 Vdd pfet_03v3 L={mirL} W={mirW} nf=1 ad='int((nf+1)/2) * W/nf * 0.18u' as='int((nf+2)/2) * W/nf * 0.18u'
+ pd='2*int((nf+1)/2) * (W/nf + 0.18u)' ps='2*int((nf+2)/2) * (W/nf + 0.18u)' nrd='0.18u / W' nrs='0.18u / W'
+ sa=0 sb=0 sd=0 m=1
XM6 net10 VPCas Vdd Vdd pfet_03v3 L={casL} W={casW} nf=1 ad='int((nf+1)/2) * W/nf * 0.18u' as='int((nf+2)/2) * W/nf * 0.18u'
+ pd='2*int((nf+1)/2) * (W/nf + 0.18u)' ps='2*int((nf+2)/2) * (W/nf + 0.18u)' nrd='0.18u / W' nrs='0.18u / W'
+ sa=0 sb=0 sd=0 m=1
XM8 Vcx VPMir net10 Vdd pfet_03v3 L={mirL} W={mirW} nf=1 ad='int((nf+1)/2) * W/nf * 0.18u' as='int((nf+2)/2) * W/nf * 0.18u'
+ pd='2*int((nf+1)/2) * (W/nf + 0.18u)' ps='2*int((nf+2)/2) * (W/nf + 0.18u)' nrd='0.18u / W' nrs='0.18u / W'
+ sa=0 sb=0 sd=0 m=1
XM15 net11 VPCas Vdd Vdd pfet_03v3 L={casL} W={casW} nf=1 ad='int((nf+1)/2) * W/nf * 0.18u' as='int((nf+2)/2) * W/nf * 0.18u'
+ pd='2*int((nf+1)/2) * (W/nf + 0.18u)' ps='2*int((nf+2)/2) * (W/nf + 0.18u)' nrd='0.18u / W' nrs='0.18u / W'
+ sa=0 sb=0 sd=0 m=1
XM16 Vcx VPMir net11 Vdd pfet_03v3 L={mirL} W={mirW} nf=1 ad='int((nf+1)/2) * W/nf * 0.18u' as='int((nf+2)/2) * W/nf * 0.18u'
+ pd='2*int((nf+1)/2) * (W/nf + 0.18u)' ps='2*int((nf+2)/2) * (W/nf + 0.18u)' nrd='0.18u / W' nrs='0.18u / W'
+ sa=0 sb=0 sd=0 m=1
XM17 net12 VPCas Vdd Vdd pfet_03v3 L={casL} W={casW} nf=1 ad='int((nf+1)/2) * W/nf * 0.18u' as='int((nf+2)/2) * W/nf * 0.18u'
+ pd='2*int((nf+1)/2) * (W/nf + 0.18u)' ps='2*int((nf+2)/2) * (W/nf + 0.18u)' nrd='0.18u / W' nrs='0.18u / W'
+ sa=0 sb=0 sd=0 m=1
XM18 Vcx VPMir net12 Vdd pfet_03v3 L={mirL} W={mirW} nf=1 ad='int((nf+1)/2) * W/nf * 0.18u' as='int((nf+2)/2) * W/nf * 0.18u'
+ pd='2*int((nf+1)/2) * (W/nf + 0.18u)' ps='2*int((nf+2)/2) * (W/nf + 0.18u)' nrd='0.18u / W' nrs='0.18u / W'
+ sa=0 sb=0 sd=0 m=1
XM2 VPMir VNMir net13 0 nfet_03v3 L=1u W=2u nf=1 ad='int((nf+1)/2) * W/nf * 0.18u' as='int((nf+2)/2) * W/nf * 0.18u'
+ pd='2*int((nf+1)/2) * (W/nf + 0.18u)' ps='2*int((nf+2)/2) * (W/nf + 0.18u)' nrd='0.18u / W' nrs='0.18u / W'
+ sa=0 sb=0 sd=0 m=1
XM3 VPMir VPMir net14 Vdd pfet_03v3 L={mirL} W={mirW} nf=1 ad='int((nf+1)/2) * W/nf * 0.18u' as='int((nf+2)/2) * W/nf * 0.18u'
+ pd='2*int((nf+1)/2) * (W/nf + 0.18u)' ps='2*int((nf+2)/2) * (W/nf + 0.18u)' nrd='0.18u / W' nrs='0.18u / W'
+ sa=0 sb=0 sd=0 m=1
XM19 net13 VNCas 0 0 nfet_03v3 L=1u W=2u nf=1 ad='int((nf+1)/2) * W/nf * 0.18u' as='int((nf+2)/2) * W/nf * 0.18u'
+ pd='2*int((nf+1)/2) * (W/nf + 0.18u)' ps='2*int((nf+2)/2) * (W/nf + 0.18u)' nrd='0.18u / W' nrs='0.18u / W'
+ sa=0 sb=0 sd=0 m=1
XM25 net14 VPCas Vdd Vdd pfet_03v3 L={casL} W={casW} nf=1 ad='int((nf+1)/2) * W/nf * 0.18u' as='int((nf+2)/2) * W/nf * 0.18u'
+ pd='2*int((nf+1)/2) * (W/nf + 0.18u)' ps='2*int((nf+2)/2) * (W/nf + 0.18u)' nrd='0.18u / W' nrs='0.18u / W'
+ sa=0 sb=0 sd=0 m=1
x2 Vdd VcbP VcbRef VcbP IB10 ota5_ab_buf_v1
x3 Vdd VcbN VcbRef VcbN IB10 ota5_ab_buf_v1
VinN net17 net18 0
.save i(vinn)
x5 net17 VinN Vdd cmos_buf
VinP net19 net20 0
.save i(vinp)
x4 net19 VinP Vdd cmos_buf
XM26 net15 VNMir net16 0 nfet_03v3 L=1u W=2u nf=1 ad='int((nf+1)/2) * W/nf * 0.18u' as='int((nf+2)/2) * W/nf * 0.18u'
+ pd='2*int((nf+1)/2) * (W/nf + 0.18u)' ps='2*int((nf+2)/2) * (W/nf + 0.18u)' nrd='0.18u / W' nrs='0.18u / W'
+ sa=0 sb=0 sd=0 m=1
XM27 net16 VNCas 0 0 nfet_03v3 L=1u W=2u nf=1 ad='int((nf+1)/2) * W/nf * 0.18u' as='int((nf+2)/2) * W/nf * 0.18u'
+ pd='2*int((nf+1)/2) * (W/nf + 0.18u)' ps='2*int((nf+2)/2) * (W/nf + 0.18u)' nrd='0.18u / W' nrs='0.18u / W'
+ sa=0 sb=0 sd=0 m=1
XM28 net15 net15 Vdd Vdd pfet_03v3 L=1u W=8u nf=1 ad='int((nf+1)/2) * W/nf * 0.18u' as='int((nf+2)/2) * W/nf * 0.18u'
+ pd='2*int((nf+1)/2) * (W/nf + 0.18u)' ps='2*int((nf+2)/2) * (W/nf + 0.18u)' nrd='0.18u / W' nrs='0.18u / W'
+ sa=0 sb=0 sd=0 m=1
XM29 IB10 net15 Vdd Vdd pfet_03v3 L=1u W=8u nf=1 ad='int((nf+1)/2) * W/nf * 0.18u' as='int((nf+2)/2) * W/nf * 0.18u'
+ pd='2*int((nf+1)/2) * (W/nf + 0.18u)' ps='2*int((nf+2)/2) * (W/nf + 0.18u)' nrd='0.18u / W' nrs='0.18u / W'
+ sa=0 sb=0 sd=0 m=1
XM30 IB10 IB10 0 0 nfet_03v3 L=1u W=8u nf=1 ad='int((nf+1)/2) * W/nf * 0.18u' as='int((nf+2)/2) * W/nf * 0.18u'
+ pd='2*int((nf+1)/2) * (W/nf + 0.18u)' ps='2*int((nf+2)/2) * (W/nf + 0.18u)' nrd='0.18u / W' nrs='0.18u / W'
+ sa=0 sb=0 sd=0 m=1
XR3 net18 VinNDr Vdd ppolyf_u_1k r_width=1e-6 r_length=1e-6 m=1
XR2 VinPDr net20 Vdd ppolyf_u_1k r_width=1e-6 r_length=1e-6 m=1
XC4 VPMir 0 cap_mim_2f0_m3m4_noshield c_width=25e-6 c_length=20e-6 m=1
XC2 IB10 0 cap_mim_2f0_m3m4_noshield c_width=25e-6 c_length=20e-6 m=1
XC7 Vdd 0 cap_mim_2f0_m3m4_noshield c_width=25e-6 c_length=20e-6 m=1
.ends


* expanding   symbol:  cellv9/clamp.sym # of pins=3
** sym_path: blocks/dac/cellv9/clamp.sym
** sch_path: blocks/dac/cellv9/clamp.sch
.subckt clamp VH Vdd VL
*.opin VH
*.opin VL
*.ipin Vdd
XM49 VL FB 0 0 nfet_03v3 L=0.28u W=2u nf=1 ad='int((nf+1)/2) * W/nf * 0.18u' as='int((nf+2)/2) * W/nf * 0.18u'
+ pd='2*int((nf+1)/2) * (W/nf + 0.18u)' ps='2*int((nf+2)/2) * (W/nf + 0.18u)' nrd='0.18u / W' nrs='0.18u / W'
+ sa=0 sb=0 sd=0 m=1
XM50 VH FB Vdd Vdd pfet_03v3 L=0.28u W=4u nf=1 ad='int((nf+1)/2) * W/nf * 0.18u' as='int((nf+2)/2) * W/nf * 0.18u'
+ pd='2*int((nf+1)/2) * (W/nf + 0.18u)' ps='2*int((nf+2)/2) * (W/nf + 0.18u)' nrd='0.18u / W' nrs='0.18u / W'
+ sa=0 sb=0 sd=0 m=1
XR3 VL FB Vdd ppolyf_u_1k r_width=1e-6 r_length=1e-6 m=1
XR1 FB VH Vdd ppolyf_u_1k r_width=1e-6 r_length=15e-6 m=1
XC2 Vdd VH cap_mim_2f0_m3m4_noshield c_width=25e-6 c_length=20e-6 m=1
XC1 Vdd VH cap_mim_2f0_m3m4_noshield c_width=10e-6 c_length=5e-6 m=1
XC3 Vdd VH cap_mim_2f0_m3m4_noshield c_width=5e-6 c_length=5e-6 m=1
XC4 VL 0 cap_mim_2f0_m3m4_noshield c_width=25e-6 c_length=20e-6 m=1
XC5 VL 0 cap_mim_2f0_m3m4_noshield c_width=10e-6 c_length=5e-6 m=1
XC6 VL 0 cap_mim_2f0_m3m4_noshield c_width=5e-6 c_length=5e-6 m=1
XC7 Vdd 0 cap_mim_2f0_m3m4_noshield c_width=25e-6 c_length=20e-6 m=1
XC8 FB 0 cap_mim_2f0_m3m4_noshield c_width=10e-6 c_length=5e-6 m=8
.ends


* expanding   symbol:  cellv9/ota5_ab_buf_v1.sym # of pins=5
** sym_path: blocks/dac/cellv9/ota5_ab_buf_v1.sym
** sch_path: blocks/dac/cellv9/ota5_ab_buf_v1.sch
.subckt ota5_ab_buf_v1 Vdd VinN VinP Vout IB10
*.opin Vout
*.ipin VinP
*.ipin VinN
*.ipin Vdd
*.ipin IB10
XM16 VoOTA net2 0 0 nfet_03v3 L=1u W=10u nf=1 ad='int((nf+1)/2) * W/nf * 0.18u' as='int((nf+2)/2) * W/nf * 0.18u'
+ pd='2*int((nf+1)/2) * (W/nf + 0.18u)' ps='2*int((nf+2)/2) * (W/nf + 0.18u)' nrd='0.18u / W' nrs='0.18u / W'
+ sa=0 sb=0 sd=0 m=1
XM18 VoOTA VinN net1 Vdd pfet_03v3 L=1u W=20u nf=1 ad='int((nf+1)/2) * W/nf * 0.18u' as='int((nf+2)/2) * W/nf * 0.18u'
+ pd='2*int((nf+1)/2) * (W/nf + 0.18u)' ps='2*int((nf+2)/2) * (W/nf + 0.18u)' nrd='0.18u / W' nrs='0.18u / W'
+ sa=0 sb=0 sd=0 m=1
XM19 net2 VinP net1 Vdd pfet_03v3 L=1u W=20u nf=1 ad='int((nf+1)/2) * W/nf * 0.18u' as='int((nf+2)/2) * W/nf * 0.18u'
+ pd='2*int((nf+1)/2) * (W/nf + 0.18u)' ps='2*int((nf+2)/2) * (W/nf + 0.18u)' nrd='0.18u / W' nrs='0.18u / W'
+ sa=0 sb=0 sd=0 m=1
XM22 net2 net2 0 0 nfet_03v3 L=1u W=10u nf=1 ad='int((nf+1)/2) * W/nf * 0.18u' as='int((nf+2)/2) * W/nf * 0.18u'
+ pd='2*int((nf+1)/2) * (W/nf + 0.18u)' ps='2*int((nf+2)/2) * (W/nf + 0.18u)' nrd='0.18u / W' nrs='0.18u / W'
+ sa=0 sb=0 sd=0 m=1
XM1 net1 net3 Vdd Vdd pfet_03v3 L=1u W=40u nf=1 ad='int((nf+1)/2) * W/nf * 0.18u' as='int((nf+2)/2) * W/nf * 0.18u'
+ pd='2*int((nf+1)/2) * (W/nf + 0.18u)' ps='2*int((nf+2)/2) * (W/nf + 0.18u)' nrd='0.18u / W' nrs='0.18u / W'
+ sa=0 sb=0 sd=0 m=1
XM2 net3 net3 Vdd Vdd pfet_03v3 L=1u W=40u nf=1 ad='int((nf+1)/2) * W/nf * 0.18u' as='int((nf+2)/2) * W/nf * 0.18u'
+ pd='2*int((nf+1)/2) * (W/nf + 0.18u)' ps='2*int((nf+2)/2) * (W/nf + 0.18u)' nrd='0.18u / W' nrs='0.18u / W'
+ sa=0 sb=0 sd=0 m=1
XM3 VI1b VI1a VI2 Vdd pfet_03v3 L=0.5u W=40u nf=1 ad='int((nf+1)/2) * W/nf * 0.18u' as='int((nf+2)/2) * W/nf * 0.18u'
+ pd='2*int((nf+1)/2) * (W/nf + 0.18u)' ps='2*int((nf+2)/2) * (W/nf + 0.18u)' nrd='0.18u / W' nrs='0.18u / W'
+ sa=0 sb=0 sd=0 m=1
XM4 VI2 VoOTA Vout 0 nfet_03v3 L=0.5u W=80u nf=1 ad='int((nf+1)/2) * W/nf * 0.18u' as='int((nf+2)/2) * W/nf * 0.18u'
+ pd='2*int((nf+1)/2) * (W/nf + 0.18u)' ps='2*int((nf+2)/2) * (W/nf + 0.18u)' nrd='0.18u / W' nrs='0.18u / W'
+ sa=0 sb=0 sd=0 m=1
XM5 Vout VI2 Vdd Vdd pfet_03v3 L=1u W=80u nf=1 ad='int((nf+1)/2) * W/nf * 0.18u' as='int((nf+2)/2) * W/nf * 0.18u'
+ pd='2*int((nf+1)/2) * (W/nf + 0.18u)' ps='2*int((nf+2)/2) * (W/nf + 0.18u)' nrd='0.18u / W' nrs='0.18u / W'
+ sa=0 sb=0 sd=0 m=1
XM6 Vout VI1b 0 0 nfet_03v3 L=0.5u W=40u nf=1 ad='int((nf+1)/2) * W/nf * 0.18u' as='int((nf+2)/2) * W/nf * 0.18u'
+ pd='2*int((nf+1)/2) * (W/nf + 0.18u)' ps='2*int((nf+2)/2) * (W/nf + 0.18u)' nrd='0.18u / W' nrs='0.18u / W'
+ sa=0 sb=0 sd=0 m=1
XM7 VI1a VI1a VI0 Vdd pfet_03v3 L=0.5u W=40u nf=1 ad='int((nf+1)/2) * W/nf * 0.18u' as='int((nf+2)/2) * W/nf * 0.18u'
+ pd='2*int((nf+1)/2) * (W/nf + 0.18u)' ps='2*int((nf+2)/2) * (W/nf + 0.18u)' nrd='0.18u / W' nrs='0.18u / W'
+ sa=0 sb=0 sd=0 m=1
XM8 VI1a VI0 Vdd Vdd pfet_03v3 L=1u W=80u nf=1 ad='int((nf+1)/2) * W/nf * 0.18u' as='int((nf+2)/2) * W/nf * 0.18u'
+ pd='2*int((nf+1)/2) * (W/nf + 0.18u)' ps='2*int((nf+2)/2) * (W/nf + 0.18u)' nrd='0.18u / W' nrs='0.18u / W'
+ sa=0 sb=0 sd=0 m=1
XM11 VI0 net4 Vdd Vdd pfet_03v3 L=0.5u W=80u nf=1 ad='int((nf+1)/2) * W/nf * 0.18u' as='int((nf+2)/2) * W/nf * 0.18u'
+ pd='2*int((nf+1)/2) * (W/nf + 0.18u)' ps='2*int((nf+2)/2) * (W/nf + 0.18u)' nrd='0.18u / W' nrs='0.18u / W'
+ sa=0 sb=0 sd=0 m=1
XM12 net4 net4 Vdd Vdd pfet_03v3 L=0.5u W=80u nf=1 ad='int((nf+1)/2) * W/nf * 0.18u' as='int((nf+2)/2) * W/nf * 0.18u'
+ pd='2*int((nf+1)/2) * (W/nf + 0.18u)' ps='2*int((nf+2)/2) * (W/nf + 0.18u)' nrd='0.18u / W' nrs='0.18u / W'
+ sa=0 sb=0 sd=0 m=1
XM9 VI2 net4 Vdd Vdd pfet_03v3 L=0.5u W=80u nf=1 ad='int((nf+1)/2) * W/nf * 0.18u' as='int((nf+2)/2) * W/nf * 0.18u'
+ pd='2*int((nf+1)/2) * (W/nf + 0.18u)' ps='2*int((nf+2)/2) * (W/nf + 0.18u)' nrd='0.18u / W' nrs='0.18u / W'
+ sa=0 sb=0 sd=0 m=1
XM10 net5 net5 Vdd Vdd pfet_03v3 L=0.5u W=40u nf=1 ad='int((nf+1)/2) * W/nf * 0.18u' as='int((nf+2)/2) * W/nf * 0.18u'
+ pd='2*int((nf+1)/2) * (W/nf + 0.18u)' ps='2*int((nf+2)/2) * (W/nf + 0.18u)' nrd='0.18u / W' nrs='0.18u / W'
+ sa=0 sb=0 sd=0 m=1
XM15 IB30Ref net5 Vdd Vdd pfet_03v3 L=0.5u W=40u nf=1 ad='int((nf+1)/2) * W/nf * 0.18u' as='int((nf+2)/2) * W/nf * 0.18u'
+ pd='2*int((nf+1)/2) * (W/nf + 0.18u)' ps='2*int((nf+2)/2) * (W/nf + 0.18u)' nrd='0.18u / W' nrs='0.18u / W'
+ sa=0 sb=0 sd=0 m=1
XM17 IB30Ref IB30Ref 0 0 nfet_03v3 L=0.5u W=40u nf=1 ad='int((nf+1)/2) * W/nf * 0.18u' as='int((nf+2)/2) * W/nf * 0.18u'
+ pd='2*int((nf+1)/2) * (W/nf + 0.18u)' ps='2*int((nf+2)/2) * (W/nf + 0.18u)' nrd='0.18u / W' nrs='0.18u / W'
+ sa=0 sb=0 sd=0 m=1
XM20 VI1a IB30Ref 0 0 nfet_03v3 L=0.5u W=40u nf=1 ad='int((nf+1)/2) * W/nf * 0.18u' as='int((nf+2)/2) * W/nf * 0.18u'
+ pd='2*int((nf+1)/2) * (W/nf + 0.18u)' ps='2*int((nf+2)/2) * (W/nf + 0.18u)' nrd='0.18u / W' nrs='0.18u / W'
+ sa=0 sb=0 sd=0 m=1
XM21 VI1b IB30Ref 0 0 nfet_03v3 L=0.5u W=40u nf=1 ad='int((nf+1)/2) * W/nf * 0.18u' as='int((nf+2)/2) * W/nf * 0.18u'
+ pd='2*int((nf+1)/2) * (W/nf + 0.18u)' ps='2*int((nf+2)/2) * (W/nf + 0.18u)' nrd='0.18u / W' nrs='0.18u / W'
+ sa=0 sb=0 sd=0 m=2
XM13 net4 IB30Ref 0 0 nfet_03v3 L=0.5u W=40u nf=1 ad='int((nf+1)/2) * W/nf * 0.18u' as='int((nf+2)/2) * W/nf * 0.18u'
+ pd='2*int((nf+1)/2) * (W/nf + 0.18u)' ps='2*int((nf+2)/2) * (W/nf + 0.18u)' nrd='0.18u / W' nrs='0.18u / W'
+ sa=0 sb=0 sd=0 m=2
XM30 net3 IB10 0 0 nfet_03v3 L=1u W=8u nf=1 ad='int((nf+1)/2) * W/nf * 0.18u' as='int((nf+2)/2) * W/nf * 0.18u'
+ pd='2*int((nf+1)/2) * (W/nf + 0.18u)' ps='2*int((nf+2)/2) * (W/nf + 0.18u)' nrd='0.18u / W' nrs='0.18u / W'
+ sa=0 sb=0 sd=0 m=2
XM14 net5 IB10 0 0 nfet_03v3 L=1u W=8u nf=1 ad='int((nf+1)/2) * W/nf * 0.18u' as='int((nf+2)/2) * W/nf * 0.18u'
+ pd='2*int((nf+1)/2) * (W/nf + 0.18u)' ps='2*int((nf+2)/2) * (W/nf + 0.18u)' nrd='0.18u / W' nrs='0.18u / W'
+ sa=0 sb=0 sd=0 m=3
**** begin user architecture code


.include /foss/pdks/gf180mcuD/libs.tech/ngspice/design.ngspice typical
.lib /foss/pdks/gf180mcuD/libs.tech/ngspice/sm141064.ngspice typical
.lib /foss/pdks/gf180mcuD/libs.tech/ngspice/sm141064.ngspice res_typical
.lib /foss/pdks/gf180mcuD/libs.tech/ngspice/sm141064.ngspice mimcap_typical


**** end user architecture code
.ends


* expanding   symbol:  common/cmos_buf.sym # of pins=3
** sym_path: blocks/dac/common/cmos_buf.sym
** sch_path: blocks/dac/common/cmos_buf.sch
.subckt cmos_buf ViBB Vi Vdd
*.ipin Vi
*.opin ViBB
*.ipin Vdd
XM49 ViB Vi 0 0 nfet_03v3 L=0.28u W=0.5u nf=1 ad='int((nf+1)/2) * W/nf * 0.18u' as='int((nf+2)/2) * W/nf * 0.18u'
+ pd='2*int((nf+1)/2) * (W/nf + 0.18u)' ps='2*int((nf+2)/2) * (W/nf + 0.18u)' nrd='0.18u / W' nrs='0.18u / W'
+ sa=0 sb=0 sd=0 m=1
XM50 ViB Vi Vdd Vdd pfet_03v3 L=0.28u W=1u nf=1 ad='int((nf+1)/2) * W/nf * 0.18u' as='int((nf+2)/2) * W/nf * 0.18u'
+ pd='2*int((nf+1)/2) * (W/nf + 0.18u)' ps='2*int((nf+2)/2) * (W/nf + 0.18u)' nrd='0.18u / W' nrs='0.18u / W'
+ sa=0 sb=0 sd=0 m=1
XM1 ViBB ViB 0 0 nfet_03v3 L=0.28u W=0.5u nf=1 ad='int((nf+1)/2) * W/nf * 0.18u' as='int((nf+2)/2) * W/nf * 0.18u'
+ pd='2*int((nf+1)/2) * (W/nf + 0.18u)' ps='2*int((nf+2)/2) * (W/nf + 0.18u)' nrd='0.18u / W' nrs='0.18u / W'
+ sa=0 sb=0 sd=0 m=1
XM2 ViBB ViB Vdd Vdd pfet_03v3 L=0.28u W=1u nf=1 ad='int((nf+1)/2) * W/nf * 0.18u' as='int((nf+2)/2) * W/nf * 0.18u'
+ pd='2*int((nf+1)/2) * (W/nf + 0.18u)' ps='2*int((nf+2)/2) * (W/nf + 0.18u)' nrd='0.18u / W' nrs='0.18u / W'
+ sa=0 sb=0 sd=0 m=1
.ends

.end
